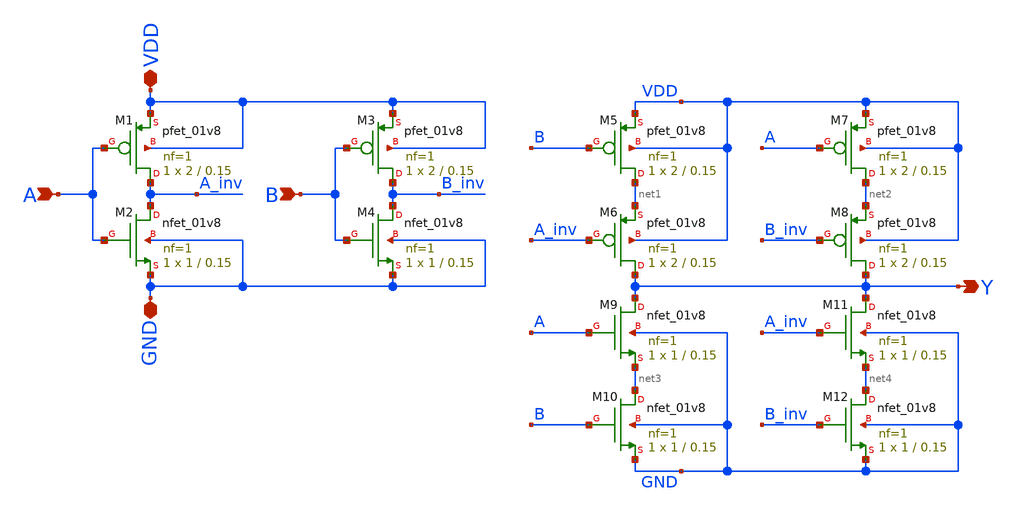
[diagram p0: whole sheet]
** sch_path: even_parity_generator/schematic/xor_12t.sch
**.subckt xor_12t A Y VDD GND B
*.ipin A
*.opin Y
*.iopin VDD
*.iopin GND
*.ipin B
XM1 A_inv A VDD VDD sky130_fd_pr__pfet_01v8 L=0.15 W=2 nf=1 ad='int((1 + 1)/2) * 2 / 1 * 0.29' as='int((1 + 2)/2) * 2 / 1 * 0.29'
+ pd='2*int((1 + 1)/2) * (2 / 1 + 0.29)' ps='2*int((1 + 2)/2) * (2 / 1 + 0.29)' nrd='0.29 / 2 ' nrs='0.29 / 2 '
+ sa=0 sb=0 sd=0 mult=1 m=1
XM2 A_inv A GND GND sky130_fd_pr__nfet_01v8 L=0.15 W=1 nf=1 ad='int((1 + 1)/2) * 1 / 1 * 0.29' as='int((1 + 2)/2) * 1 / 1 * 0.29'
+ pd='2*int((1 + 1)/2) * (1 / 1 + 0.29)' ps='2*int((1 + 2)/2) * (1 / 1 + 0.29)' nrd='0.29 / 1 ' nrs='0.29 / 1 '
+ sa=0 sb=0 sd=0 mult=1 m=1
XM3 B_inv B VDD VDD sky130_fd_pr__pfet_01v8 L=0.15 W=2 nf=1 ad='int((1 + 1)/2) * 2 / 1 * 0.29' as='int((1 + 2)/2) * 2 / 1 * 0.29'
+ pd='2*int((1 + 1)/2) * (2 / 1 + 0.29)' ps='2*int((1 + 2)/2) * (2 / 1 + 0.29)' nrd='0.29 / 2 ' nrs='0.29 / 2 '
+ sa=0 sb=0 sd=0 mult=1 m=1
XM4 B_inv B GND GND sky130_fd_pr__nfet_01v8 L=0.15 W=1 nf=1 ad='int((1 + 1)/2) * 1 / 1 * 0.29' as='int((1 + 2)/2) * 1 / 1 * 0.29'
+ pd='2*int((1 + 1)/2) * (1 / 1 + 0.29)' ps='2*int((1 + 2)/2) * (1 / 1 + 0.29)' nrd='0.29 / 1 ' nrs='0.29 / 1 '
+ sa=0 sb=0 sd=0 mult=1 m=1
XM5 net1 B VDD VDD sky130_fd_pr__pfet_01v8 L=0.15 W=2 nf=1 ad='int((1 + 1)/2) * 2 / 1 * 0.29' as='int((1 + 2)/2) * 2 / 1 * 0.29'
+ pd='2*int((1 + 1)/2) * (2 / 1 + 0.29)' ps='2*int((1 + 2)/2) * (2 / 1 + 0.29)' nrd='0.29 / 2 ' nrs='0.29 / 2 '
+ sa=0 sb=0 sd=0 mult=1 m=1
XM6 Y A_inv net1 VDD sky130_fd_pr__pfet_01v8 L=0.15 W=2 nf=1 ad='int((1 + 1)/2) * 2 / 1 * 0.29' as='int((1 + 2)/2) * 2 / 1 * 0.29'
+ pd='2*int((1 + 1)/2) * (2 / 1 + 0.29)' ps='2*int((1 + 2)/2) * (2 / 1 + 0.29)' nrd='0.29 / 2 ' nrs='0.29 / 2 '
+ sa=0 sb=0 sd=0 mult=1 m=1
XM7 net2 A VDD VDD sky130_fd_pr__pfet_01v8 L=0.15 W=2 nf=1 ad='int((1 + 1)/2) * 2 / 1 * 0.29' as='int((1 + 2)/2) * 2 / 1 * 0.29'
+ pd='2*int((1 + 1)/2) * (2 / 1 + 0.29)' ps='2*int((1 + 2)/2) * (2 / 1 + 0.29)' nrd='0.29 / 2 ' nrs='0.29 / 2 '
+ sa=0 sb=0 sd=0 mult=1 m=1
XM8 Y B_inv net2 VDD sky130_fd_pr__pfet_01v8 L=0.15 W=2 nf=1 ad='int((1 + 1)/2) * 2 / 1 * 0.29' as='int((1 + 2)/2) * 2 / 1 * 0.29'
+ pd='2*int((1 + 1)/2) * (2 / 1 + 0.29)' ps='2*int((1 + 2)/2) * (2 / 1 + 0.29)' nrd='0.29 / 2 ' nrs='0.29 / 2 '
+ sa=0 sb=0 sd=0 mult=1 m=1
XM9 Y A net3 GND sky130_fd_pr__nfet_01v8 L=0.15 W=1 nf=1 ad='int((1 + 1)/2) * 1 / 1 * 0.29' as='int((1 + 2)/2) * 1 / 1 * 0.29'
+ pd='2*int((1 + 1)/2) * (1 / 1 + 0.29)' ps='2*int((1 + 2)/2) * (1 / 1 + 0.29)' nrd='0.29 / 1 ' nrs='0.29 / 1 '
+ sa=0 sb=0 sd=0 mult=1 m=1
XM10 net3 B GND GND sky130_fd_pr__nfet_01v8 L=0.15 W=1 nf=1 ad='int((1 + 1)/2) * 1 / 1 * 0.29' as='int((1 + 2)/2) * 1 / 1 * 0.29'
+ pd='2*int((1 + 1)/2) * (1 / 1 + 0.29)' ps='2*int((1 + 2)/2) * (1 / 1 + 0.29)' nrd='0.29 / 1 ' nrs='0.29 / 1 '
+ sa=0 sb=0 sd=0 mult=1 m=1
XM11 Y A_inv net4 GND sky130_fd_pr__nfet_01v8 L=0.15 W=1 nf=1 ad='int((1 + 1)/2) * 1 / 1 * 0.29' as='int((1 + 2)/2) * 1 / 1 * 0.29'
+ pd='2*int((1 + 1)/2) * (1 / 1 + 0.29)' ps='2*int((1 + 2)/2) * (1 / 1 + 0.29)' nrd='0.29 / 1 ' nrs='0.29 / 1 '
+ sa=0 sb=0 sd=0 mult=1 m=1
XM12 net4 B_inv GND GND sky130_fd_pr__nfet_01v8 L=0.15 W=1 nf=1 ad='int((1 + 1)/2) * 1 / 1 * 0.29' as='int((1 + 2)/2) * 1 / 1 * 0.29'
+ pd='2*int((1 + 1)/2) * (1 / 1 + 0.29)' ps='2*int((1 + 2)/2) * (1 / 1 + 0.29)' nrd='0.29 / 1 ' nrs='0.29 / 1 '
+ sa=0 sb=0 sd=0 mult=1 m=1
**.ends
.end
